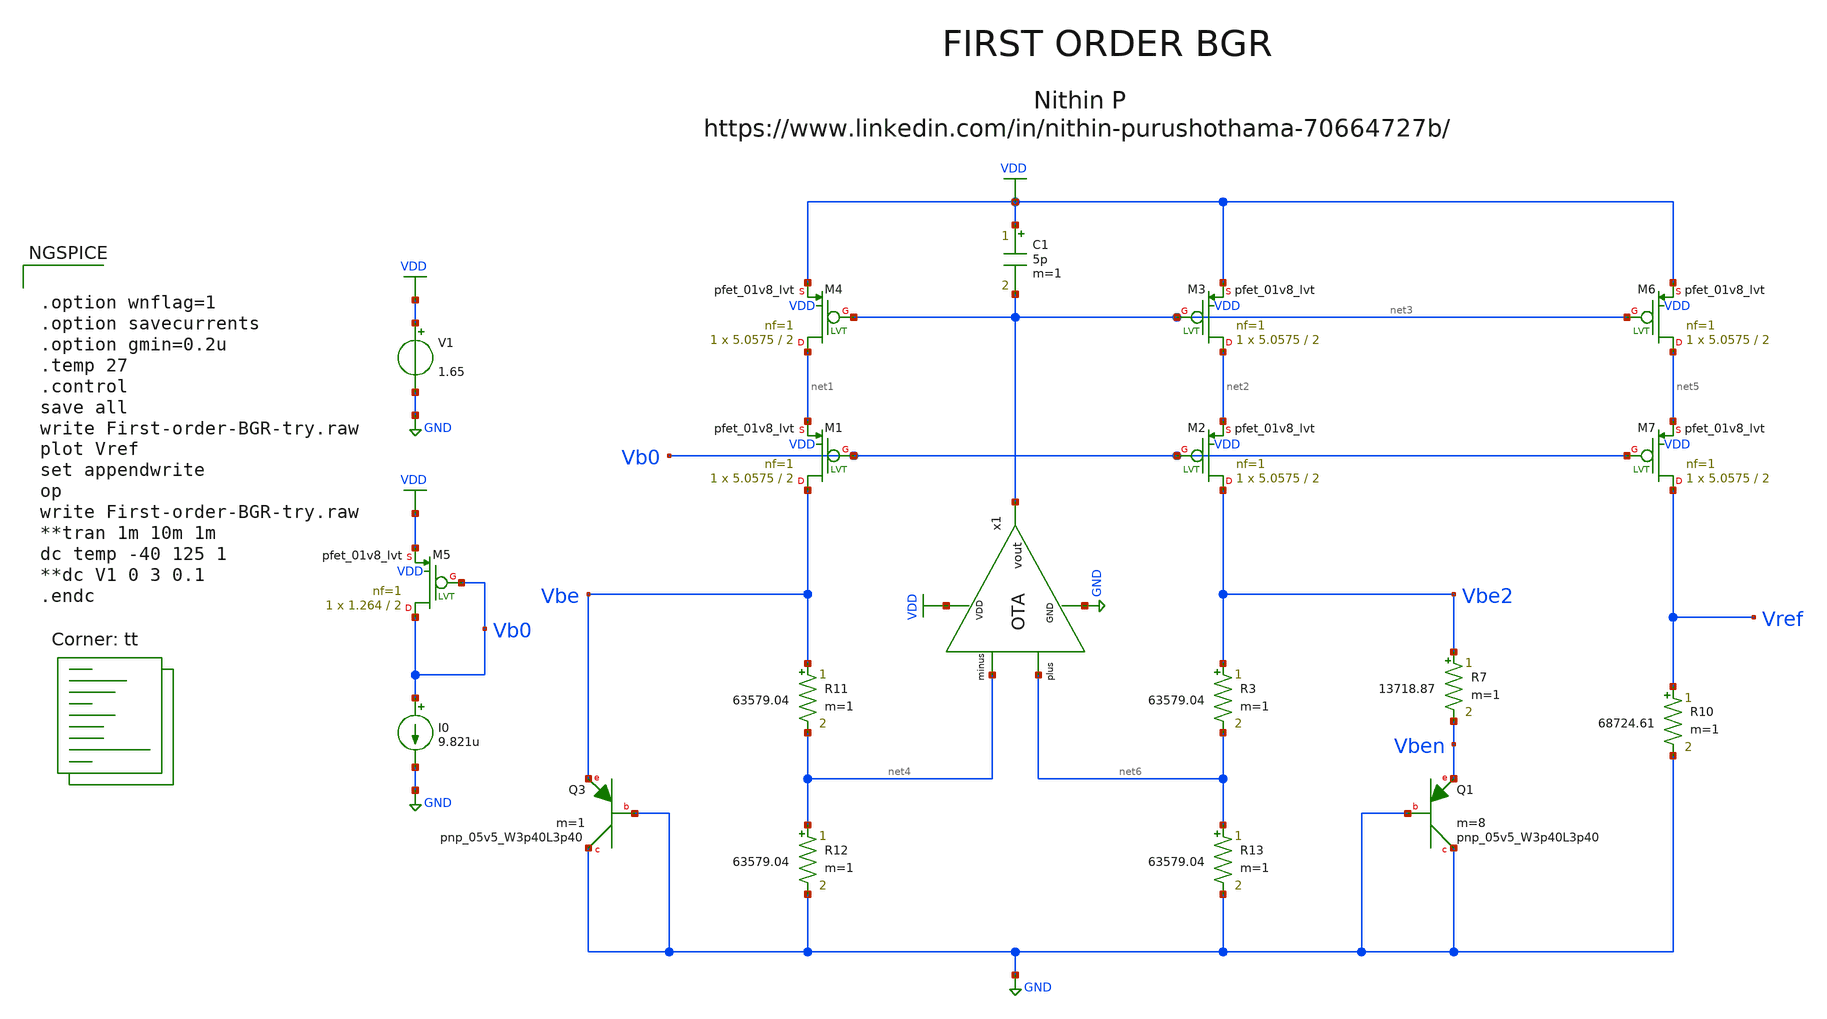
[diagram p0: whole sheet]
** sch_path: Schematic/BGR/First-order-BGR-try.sch
**.subckt First-order-BGR-try
V1 VDD GND 1.65
XQ1 GND GND Vben sky130_fd_pr__pnp_05v5_W3p40L3p40 m=8
XQ3 GND GND Vbe sky130_fd_pr__pnp_05v5_W3p40L3p40 m=1
R7 Vbe2 Vben 13718.87 m=1
x1 VDD net4 net6 net3 GND OTA
C1 VDD net3 5p m=1
R10 Vref GND 68724.61 m=1
XM1 Vbe Vb0 net1 VDD sky130_fd_pr__pfet_01v8_lvt L=2 W=5.0575 nf=1 ad='int((nf+1)/2) * W/nf * 0.29' as='int((nf+2)/2) * W/nf * 0.29'
+ pd='2*int((nf+1)/2) * (W/nf + 0.29)' ps='2*int((nf+2)/2) * (W/nf + 0.29)' nrd='0.29 / W' nrs='0.29 / W'
+ sa=0 sb=0 sd=0 mult=1 m=1
R3 Vbe2 net6 63579.04 m=1
XM2 Vbe2 Vb0 net2 VDD sky130_fd_pr__pfet_01v8_lvt L=2 W=5.0575 nf=1 ad='int((nf+1)/2) * W/nf * 0.29'
+ as='int((nf+2)/2) * W/nf * 0.29' pd='2*int((nf+1)/2) * (W/nf + 0.29)' ps='2*int((nf+2)/2) * (W/nf + 0.29)'
+ nrd='0.29 / W' nrs='0.29 / W' sa=0 sb=0 sd=0 mult=1 m=1
XM3 net2 net3 VDD VDD sky130_fd_pr__pfet_01v8_lvt L=2 W=5.0575 nf=1 ad='int((nf+1)/2) * W/nf * 0.29'
+ as='int((nf+2)/2) * W/nf * 0.29' pd='2*int((nf+1)/2) * (W/nf + 0.29)' ps='2*int((nf+2)/2) * (W/nf + 0.29)'
+ nrd='0.29 / W' nrs='0.29 / W' sa=0 sb=0 sd=0 mult=1 m=1
XM4 net1 net3 VDD VDD sky130_fd_pr__pfet_01v8_lvt L=2 W=5.0575 nf=1 ad='int((nf+1)/2) * W/nf * 0.29'
+ as='int((nf+2)/2) * W/nf * 0.29' pd='2*int((nf+1)/2) * (W/nf + 0.29)' ps='2*int((nf+2)/2) * (W/nf + 0.29)'
+ nrd='0.29 / W' nrs='0.29 / W' sa=0 sb=0 sd=0 mult=1 m=1
XM5 Vb0 Vb0 VDD VDD sky130_fd_pr__pfet_01v8_lvt L=2 W=1.264 nf=1 ad='int((nf+1)/2) * W/nf * 0.29' as='int((nf+2)/2) * W/nf * 0.29'
+ pd='2*int((nf+1)/2) * (W/nf + 0.29)' ps='2*int((nf+2)/2) * (W/nf + 0.29)' nrd='0.29 / W' nrs='0.29 / W'
+ sa=0 sb=0 sd=0 mult=1 m=1
I0 Vb0 GND 9.821u
R11 Vbe net4 63579.04 m=1
R12 net4 GND 63579.04 m=1
R13 net6 GND 63579.04 m=1
XM6 net5 net3 VDD VDD sky130_fd_pr__pfet_01v8_lvt L=2 W=5.0575 nf=1 ad='int((nf+1)/2) * W/nf * 0.29'
+ as='int((nf+2)/2) * W/nf * 0.29' pd='2*int((nf+1)/2) * (W/nf + 0.29)' ps='2*int((nf+2)/2) * (W/nf + 0.29)'
+ nrd='0.29 / W' nrs='0.29 / W' sa=0 sb=0 sd=0 mult=1 m=1
XM7 Vref Vb0 net5 VDD sky130_fd_pr__pfet_01v8_lvt L=2 W=5.0575 nf=1 ad='int((nf+1)/2) * W/nf * 0.29'
+ as='int((nf+2)/2) * W/nf * 0.29' pd='2*int((nf+1)/2) * (W/nf + 0.29)' ps='2*int((nf+2)/2) * (W/nf + 0.29)'
+ nrd='0.29 / W' nrs='0.29 / W' sa=0 sb=0 sd=0 mult=1 m=1
**** begin user architecture code


.option wnflag=1
.option savecurrents
.option gmin=0.2u
.temp 27
.control
save all
write First-order-BGR-try.raw
plot Vref
set appendwrite
op
write First-order-BGR-try.raw
**tran 1m 10m 1m
dc temp -40 125 1
**dc V1 0 3 0.1
.endc


.lib $::SKYWATER_MODELS/sky130.lib.spice tt
**** end user architecture code
**.ends
.GLOBAL VDD
.GLOBAL GND
.end
